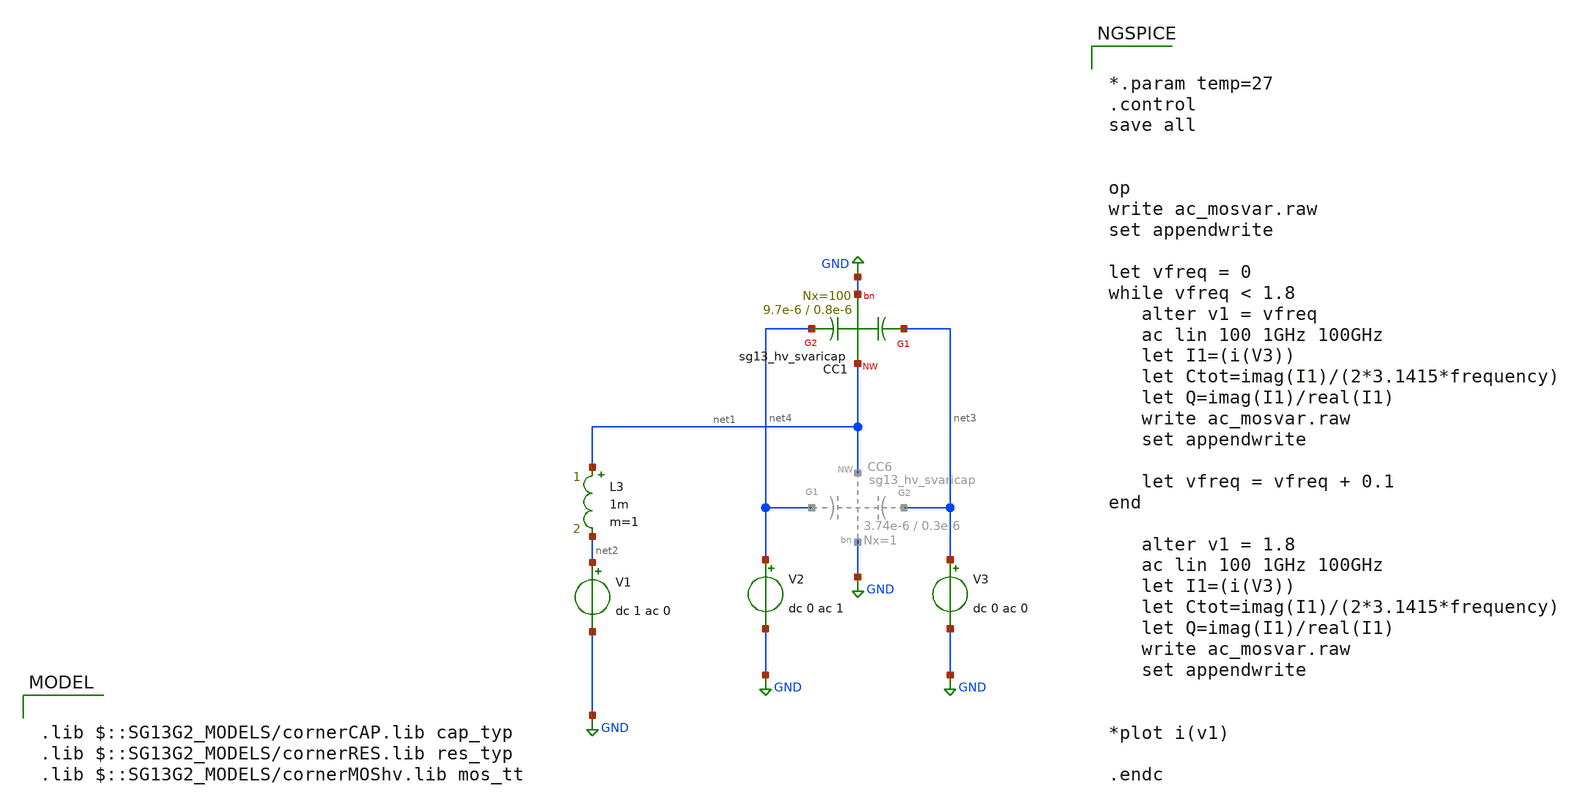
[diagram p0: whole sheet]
** sch_path: design_data/xschem/measuremenst_and_test_of_idas/ac_svaricap_test3.sch
**.subckt ac_svaricap_test3
V1 net2 GND dc 1 ac 0
L3 net1 net2 1m m=1
V3 net3 GND dc 0 ac 0
V2 net4 GND dc 0 ac 1
XC1 net3 net1 net4 GND sg13_hv_svaricap w=9.7e-6 l=0.8e-6 Nx=100
**** begin user architecture code

.lib $::SG13G2_MODELS/cornerCAP.lib cap_typ
.lib $::SG13G2_MODELS/cornerRES.lib res_typ
.lib $::SG13G2_MODELS/cornerMOShv.lib mos_tt



*.param temp=27
.control
save all


op
write ac_mosvar.raw
set appendwrite

let vfreq = 0
while vfreq < 1.8
   alter v1 = vfreq
   ac lin 100 1GHz 100GHz
   let I1=(i(V3))
   let Ctot=imag(I1)/(2*3.1415*frequency)
   let Q=imag(I1)/real(I1)
   write ac_mosvar.raw
   set appendwrite

   let vfreq = vfreq + 0.1
end

   alter v1 = 1.8
   ac lin 100 1GHz 100GHz
   let I1=(i(V3))
   let Ctot=imag(I1)/(2*3.1415*frequency)
   let Q=imag(I1)/real(I1)
   write ac_mosvar.raw
   set appendwrite


*plot i(v1)

.endc


**** end user architecture code
**.ends
.GLOBAL GND
.end
